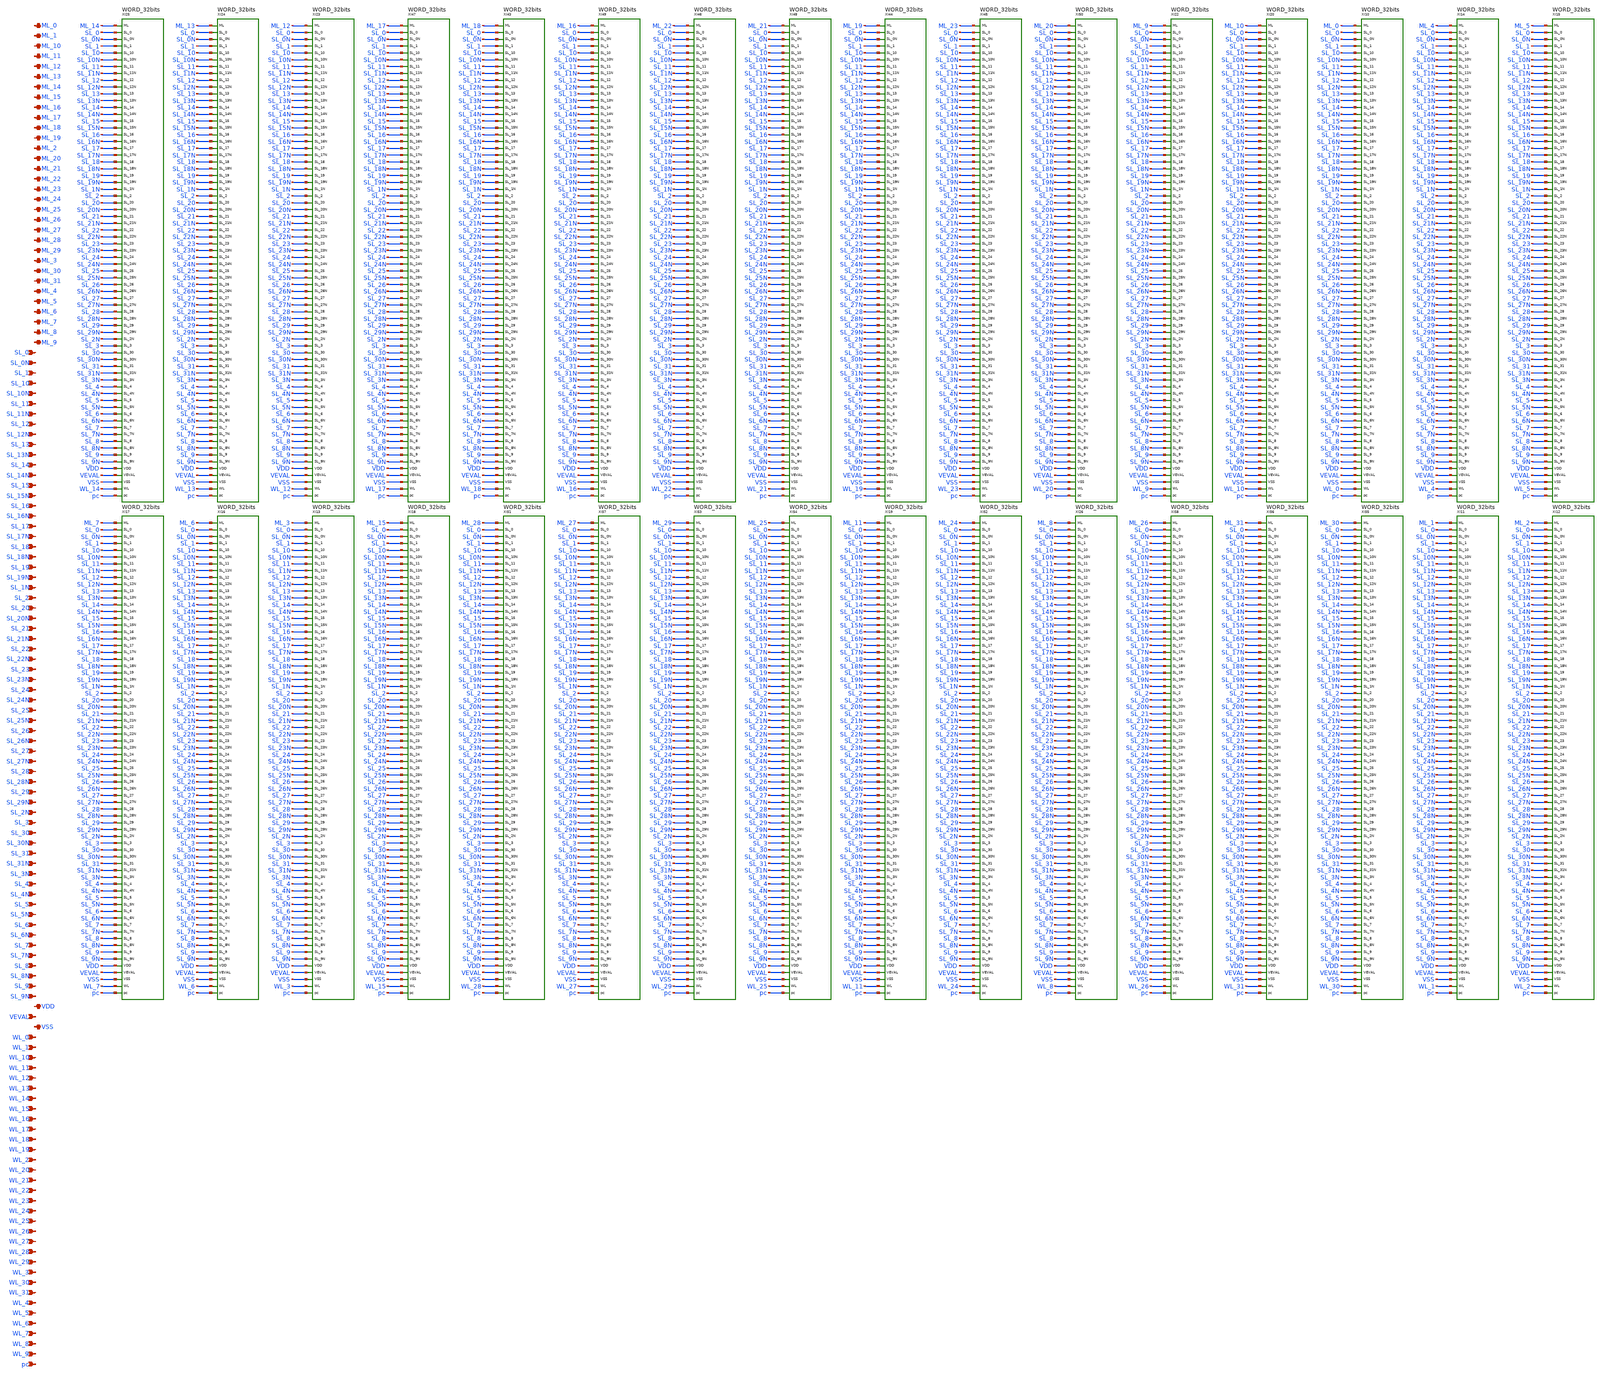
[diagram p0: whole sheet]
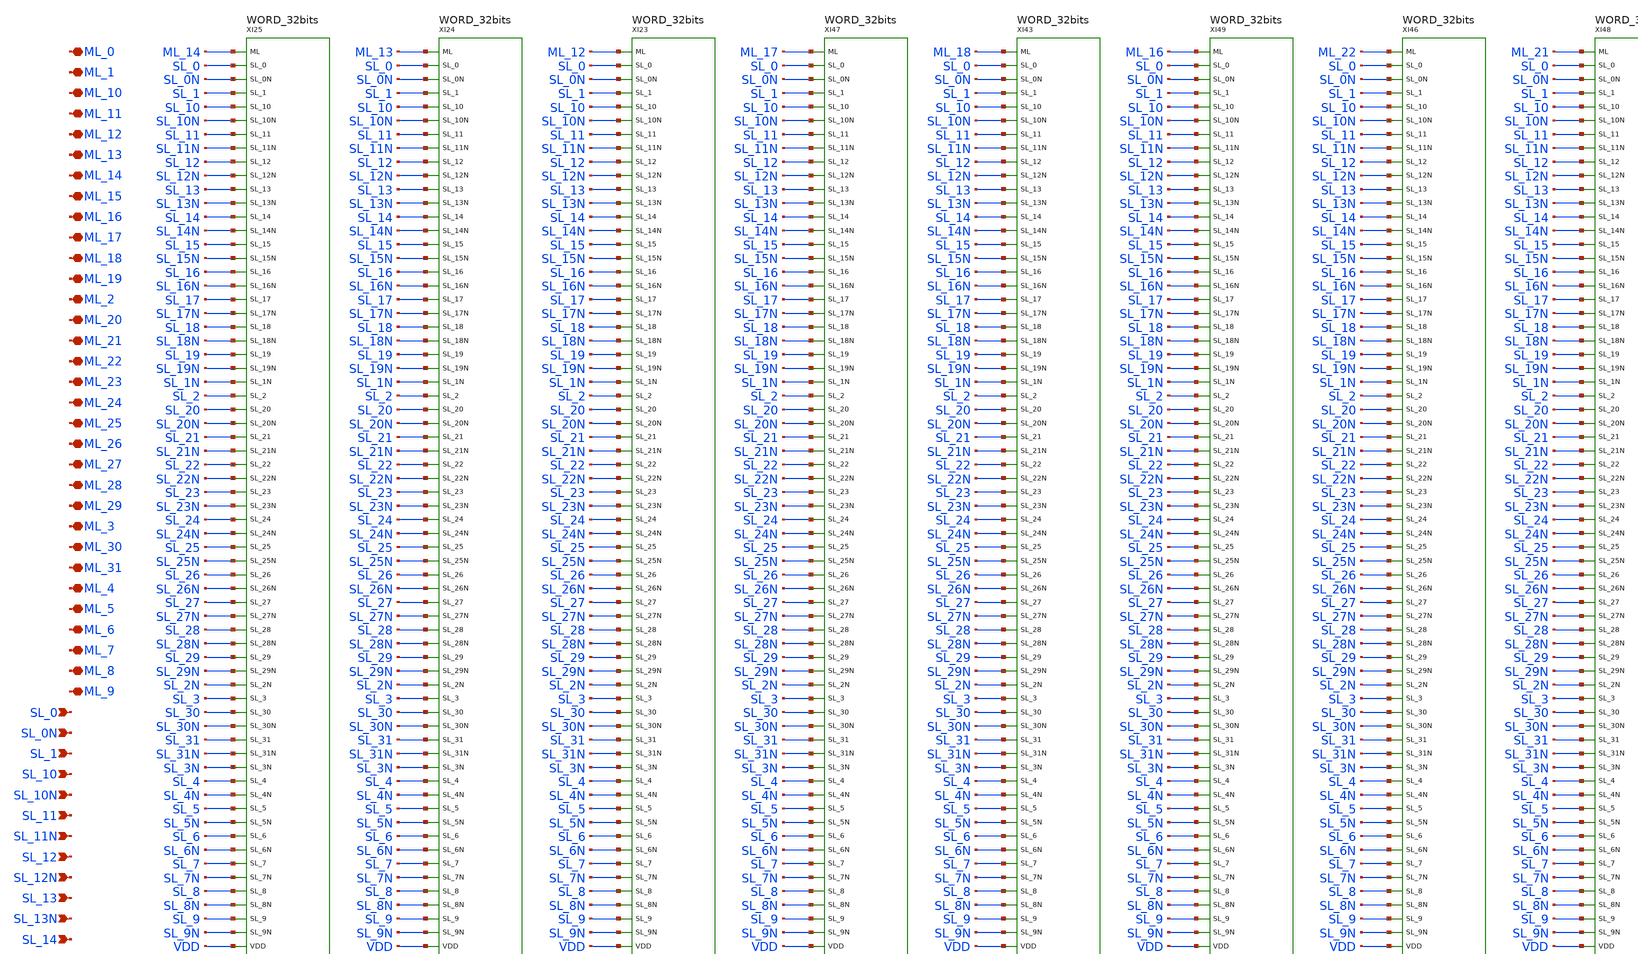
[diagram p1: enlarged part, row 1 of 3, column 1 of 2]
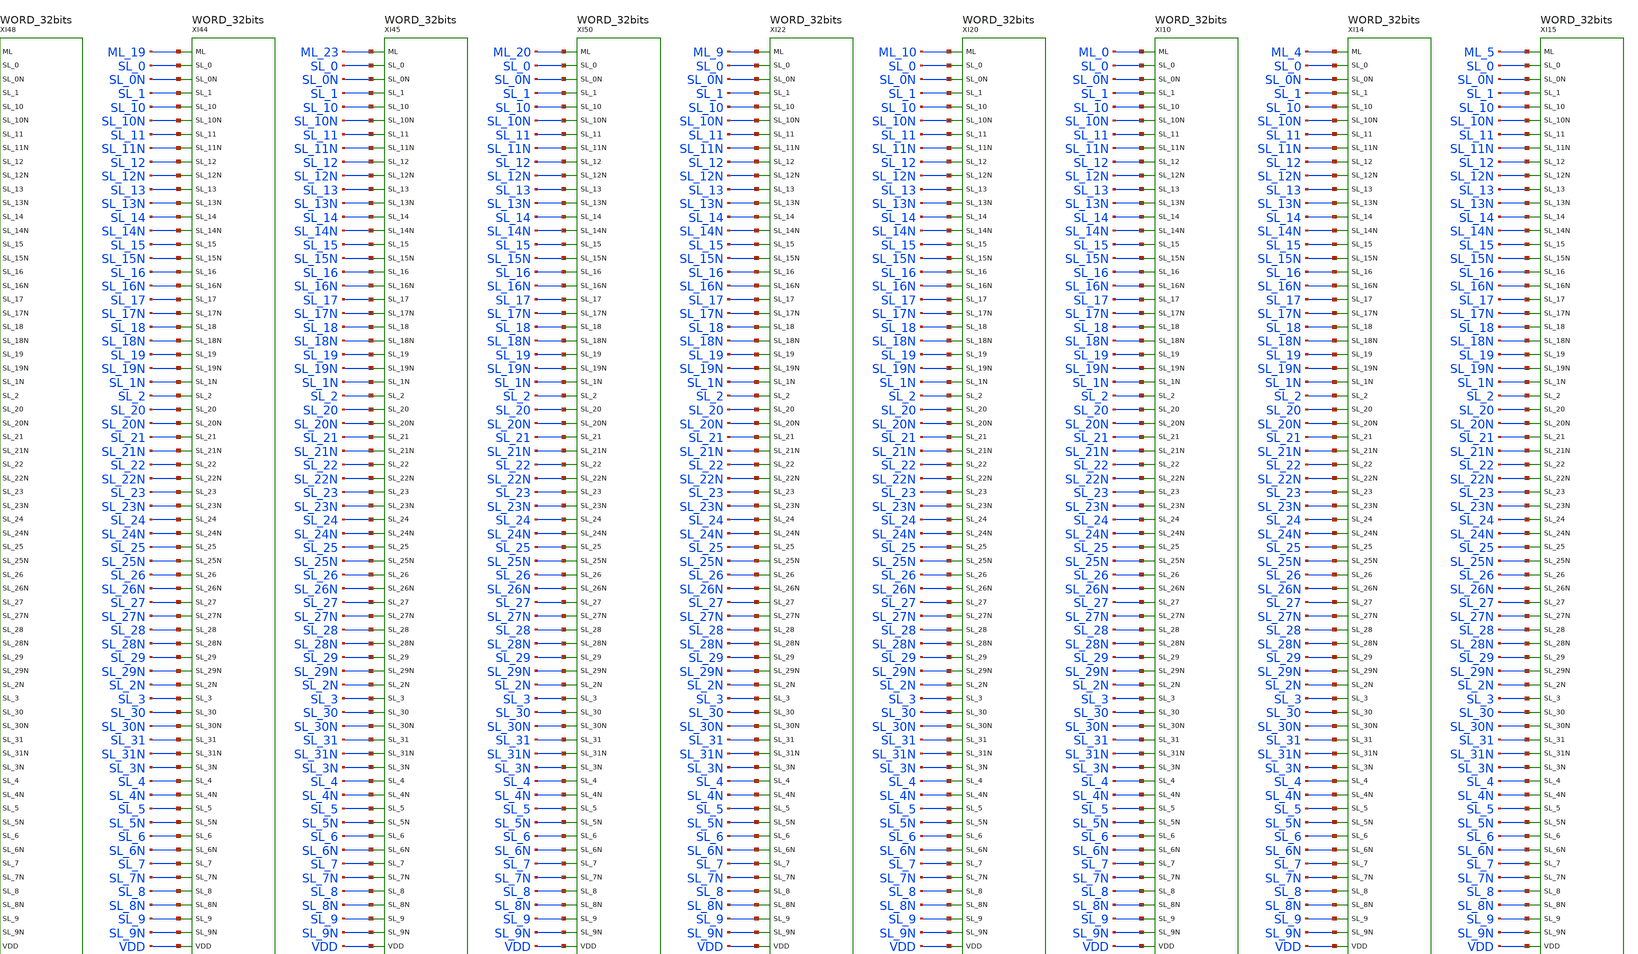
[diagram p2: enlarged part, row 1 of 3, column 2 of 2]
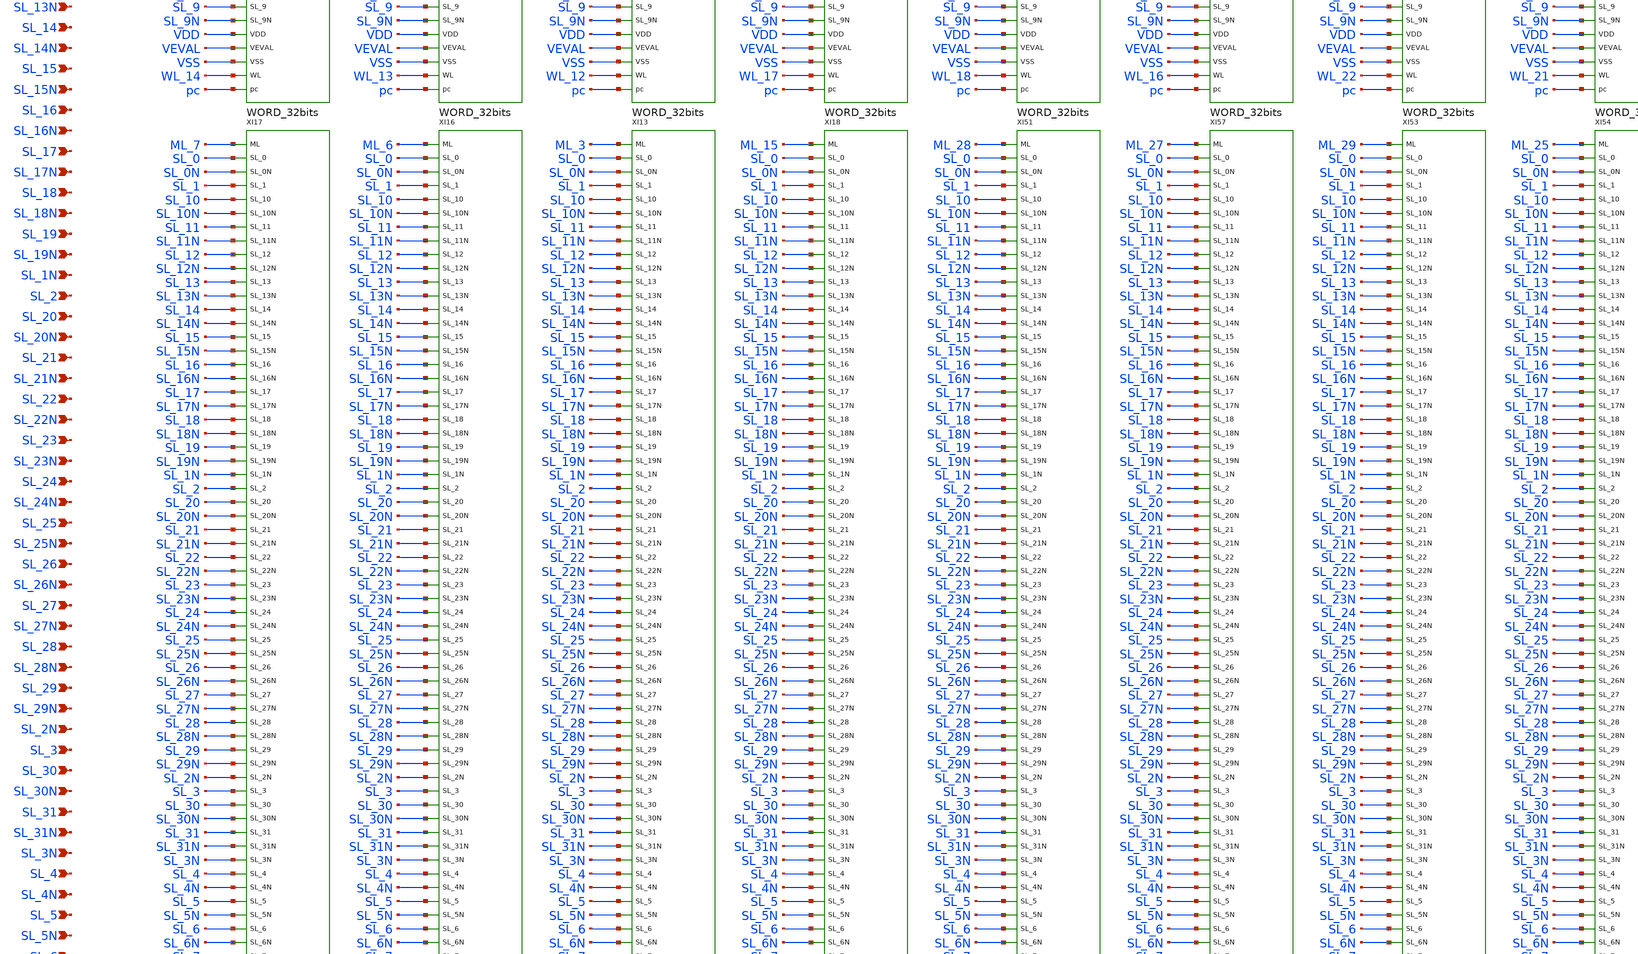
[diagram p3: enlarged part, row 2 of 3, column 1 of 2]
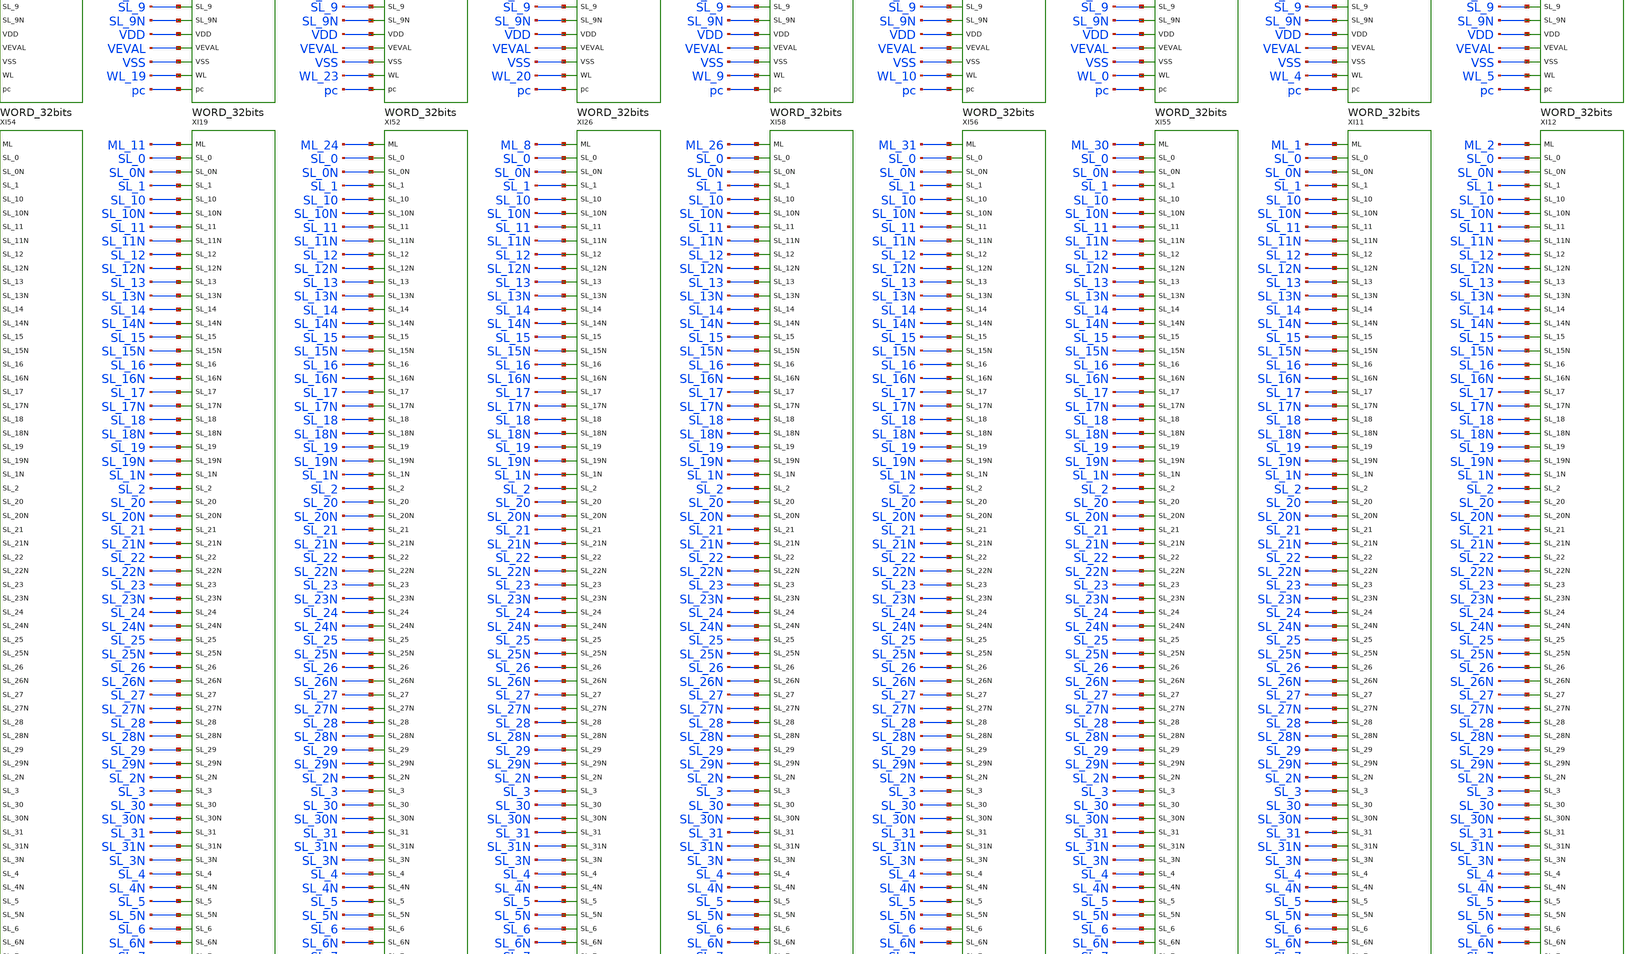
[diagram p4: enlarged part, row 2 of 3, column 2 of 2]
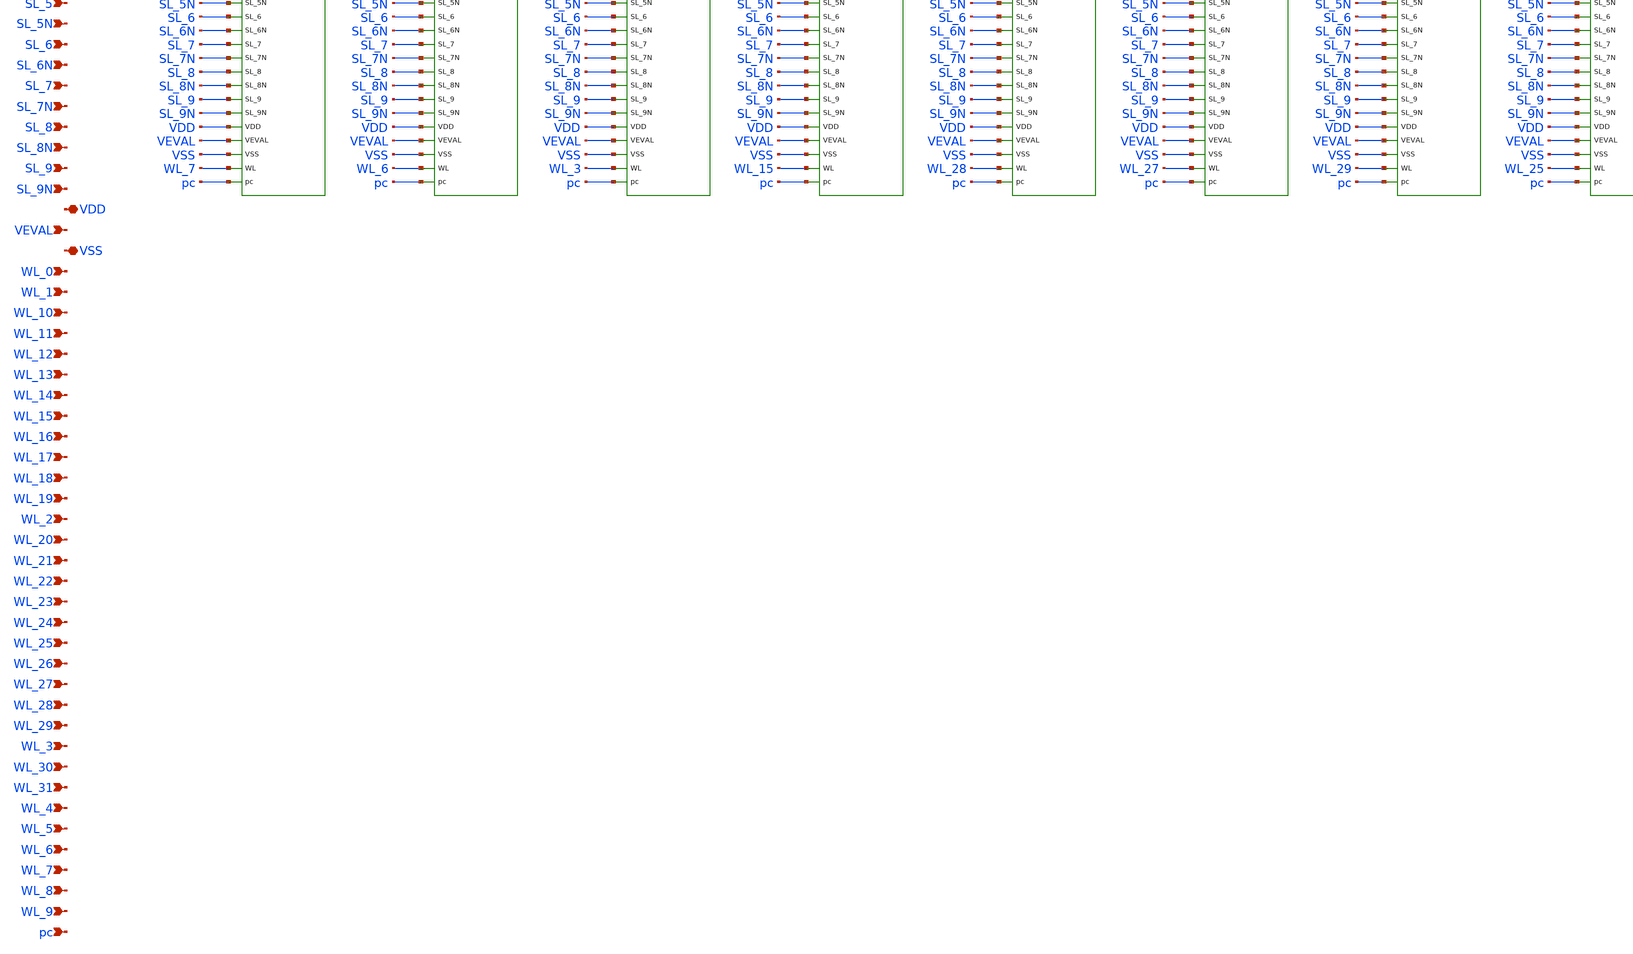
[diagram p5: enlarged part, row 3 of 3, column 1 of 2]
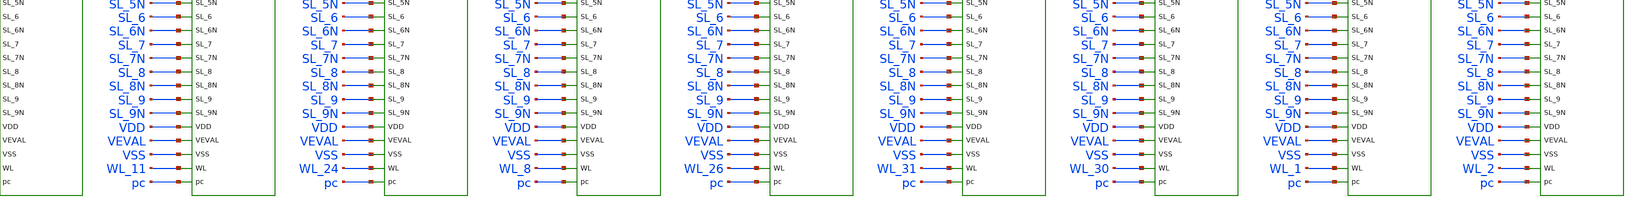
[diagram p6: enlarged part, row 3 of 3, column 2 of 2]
** sch_path: SoC6169-main/schematic/xschem/ARRAY_32x32.sch
* Copyright 2026 USFQ CAM team
* Licensed under the Apache License, Version 2.0 (the "License");
* you may not use this file except in compliance with the License.
* You may obtain a copy of the License at
* https://www.apache.org/licenses/LICENSE-2.0
* Unless required by applicable law or agreed to in writing, software
* distributed under the License is distributed on an "AS IS" BASIS,
* WITHOUT WARRANTIES OR CONDITIONS OF ANY KIND, either express or implied.
* See the License for the specific language governing permissions and
* limitations under the License.
**.subckt ARRAY_32x32 ML_0 ML_1 ML_10 ML_11 ML_12 ML_13 ML_14 ML_15 ML_16 ML_17 ML_18 ML_19 ML_2
*+ ML_20 ML_21 ML_22 ML_23 ML_24 ML_25 ML_26 ML_27 ML_28 ML_29 ML_3 ML_30 ML_31 ML_4 ML_5 ML_6 ML_7 ML_8
*+ ML_9 SL_0 SL_0N SL_1 SL_10 SL_10N SL_11 SL_11N SL_12 SL_12N SL_13 SL_13N SL_14 SL_14N SL_15 SL_15N SL_16
*+ SL_16N SL_17 SL_17N SL_18 SL_18N SL_19 SL_19N SL_1N SL_2 SL_20 SL_20N SL_21 SL_21N SL_22 SL_22N SL_23
*+ SL_23N SL_24 SL_24N SL_25 SL_25N SL_26 SL_26N SL_27 SL_27N SL_28 SL_28N SL_29 SL_29N SL_2N SL_3 SL_30
*+ SL_30N SL_31 SL_31N SL_3N SL_4 SL_4N SL_5 SL_5N SL_6 SL_6N SL_7 SL_7N SL_8 SL_8N SL_9 SL_9N VDD VEVAL VSS
*+ WL_0 WL_1 WL_10 WL_11 WL_12 WL_13 WL_14 WL_15 WL_16 WL_17 WL_18 WL_19 WL_2 WL_20 WL_21 WL_22 WL_23 WL_24
*+ WL_25 WL_26 WL_27 WL_28 WL_29 WL_3 WL_30 WL_31 WL_4 WL_5 WL_6 WL_7 WL_8 WL_9 pc
*.iopin ML_0
*.iopin ML_1
*.iopin ML_10
*.iopin ML_11
*.iopin ML_12
*.iopin ML_13
*.iopin ML_14
*.iopin ML_15
*.iopin ML_16
*.iopin ML_17
*.iopin ML_18
*.iopin ML_19
*.iopin ML_2
*.iopin ML_20
*.iopin ML_21
*.iopin ML_22
*.iopin ML_23
*.iopin ML_24
*.iopin ML_25
*.iopin ML_26
*.iopin ML_27
*.iopin ML_28
*.iopin ML_29
*.iopin ML_3
*.iopin ML_30
*.iopin ML_31
*.iopin ML_4
*.iopin ML_5
*.iopin ML_6
*.iopin ML_7
*.iopin ML_8
*.iopin ML_9
*.ipin SL_0
*.ipin SL_0N
*.ipin SL_1
*.ipin SL_10
*.ipin SL_10N
*.ipin SL_11
*.ipin SL_11N
*.ipin SL_12
*.ipin SL_12N
*.ipin SL_13
*.ipin SL_13N
*.ipin SL_14
*.ipin SL_14N
*.ipin SL_15
*.ipin SL_15N
*.ipin SL_16
*.ipin SL_16N
*.ipin SL_17
*.ipin SL_17N
*.ipin SL_18
*.ipin SL_18N
*.ipin SL_19
*.ipin SL_19N
*.ipin SL_1N
*.ipin SL_2
*.ipin SL_20
*.ipin SL_20N
*.ipin SL_21
*.ipin SL_21N
*.ipin SL_22
*.ipin SL_22N
*.ipin SL_23
*.ipin SL_23N
*.ipin SL_24
*.ipin SL_24N
*.ipin SL_25
*.ipin SL_25N
*.ipin SL_26
*.ipin SL_26N
*.ipin SL_27
*.ipin SL_27N
*.ipin SL_28
*.ipin SL_28N
*.ipin SL_29
*.ipin SL_29N
*.ipin SL_2N
*.ipin SL_3
*.ipin SL_30
*.ipin SL_30N
*.ipin SL_31
*.ipin SL_31N
*.ipin SL_3N
*.ipin SL_4
*.ipin SL_4N
*.ipin SL_5
*.ipin SL_5N
*.ipin SL_6
*.ipin SL_6N
*.ipin SL_7
*.ipin SL_7N
*.ipin SL_8
*.ipin SL_8N
*.ipin SL_9
*.ipin SL_9N
*.iopin VDD
*.ipin VEVAL
*.iopin VSS
*.ipin WL_0
*.ipin WL_1
*.ipin WL_10
*.ipin WL_11
*.ipin WL_12
*.ipin WL_13
*.ipin WL_14
*.ipin WL_15
*.ipin WL_16
*.ipin WL_17
*.ipin WL_18
*.ipin WL_19
*.ipin WL_2
*.ipin WL_20
*.ipin WL_21
*.ipin WL_22
*.ipin WL_23
*.ipin WL_24
*.ipin WL_25
*.ipin WL_26
*.ipin WL_27
*.ipin WL_28
*.ipin WL_29
*.ipin WL_3
*.ipin WL_30
*.ipin WL_31
*.ipin WL_4
*.ipin WL_5
*.ipin WL_6
*.ipin WL_7
*.ipin WL_8
*.ipin WL_9
*.ipin pc
XI25 ML_14 SL_0 SL_0N SL_1 SL_10 SL_10N SL_11 SL_11N SL_12 SL_12N SL_13 SL_13N SL_14 SL_14N SL_15
+ SL_15N SL_16 SL_16N SL_17 SL_17N SL_18 SL_18N SL_19 SL_19N SL_1N SL_2 SL_20 SL_20N SL_21 SL_21N SL_22
+ SL_22N SL_23 SL_23N SL_24 SL_24N SL_25 SL_25N SL_26 SL_26N SL_27 SL_27N SL_28 SL_28N SL_29 SL_29N SL_2N
+ SL_3 SL_30 SL_30N SL_31 SL_31N SL_3N SL_4 SL_4N SL_5 SL_5N SL_6 SL_6N SL_7 SL_7N SL_8 SL_8N SL_9 SL_9N
+ VDD VEVAL VSS WL_14 pc WORD_32bits
XI24 ML_13 SL_0 SL_0N SL_1 SL_10 SL_10N SL_11 SL_11N SL_12 SL_12N SL_13 SL_13N SL_14 SL_14N SL_15
+ SL_15N SL_16 SL_16N SL_17 SL_17N SL_18 SL_18N SL_19 SL_19N SL_1N SL_2 SL_20 SL_20N SL_21 SL_21N SL_22
+ SL_22N SL_23 SL_23N SL_24 SL_24N SL_25 SL_25N SL_26 SL_26N SL_27 SL_27N SL_28 SL_28N SL_29 SL_29N SL_2N
+ SL_3 SL_30 SL_30N SL_31 SL_31N SL_3N SL_4 SL_4N SL_5 SL_5N SL_6 SL_6N SL_7 SL_7N SL_8 SL_8N SL_9 SL_9N
+ VDD VEVAL VSS WL_13 pc WORD_32bits
XI23 ML_12 SL_0 SL_0N SL_1 SL_10 SL_10N SL_11 SL_11N SL_12 SL_12N SL_13 SL_13N SL_14 SL_14N SL_15
+ SL_15N SL_16 SL_16N SL_17 SL_17N SL_18 SL_18N SL_19 SL_19N SL_1N SL_2 SL_20 SL_20N SL_21 SL_21N SL_22
+ SL_22N SL_23 SL_23N SL_24 SL_24N SL_25 SL_25N SL_26 SL_26N SL_27 SL_27N SL_28 SL_28N SL_29 SL_29N SL_2N
+ SL_3 SL_30 SL_30N SL_31 SL_31N SL_3N SL_4 SL_4N SL_5 SL_5N SL_6 SL_6N SL_7 SL_7N SL_8 SL_8N SL_9 SL_9N
+ VDD VEVAL VSS WL_12 pc WORD_32bits
XI47 ML_17 SL_0 SL_0N SL_1 SL_10 SL_10N SL_11 SL_11N SL_12 SL_12N SL_13 SL_13N SL_14 SL_14N SL_15
+ SL_15N SL_16 SL_16N SL_17 SL_17N SL_18 SL_18N SL_19 SL_19N SL_1N SL_2 SL_20 SL_20N SL_21 SL_21N SL_22
+ SL_22N SL_23 SL_23N SL_24 SL_24N SL_25 SL_25N SL_26 SL_26N SL_27 SL_27N SL_28 SL_28N SL_29 SL_29N SL_2N
+ SL_3 SL_30 SL_30N SL_31 SL_31N SL_3N SL_4 SL_4N SL_5 SL_5N SL_6 SL_6N SL_7 SL_7N SL_8 SL_8N SL_9 SL_9N
+ VDD VEVAL VSS WL_17 pc WORD_32bits
XI43 ML_18 SL_0 SL_0N SL_1 SL_10 SL_10N SL_11 SL_11N SL_12 SL_12N SL_13 SL_13N SL_14 SL_14N SL_15
+ SL_15N SL_16 SL_16N SL_17 SL_17N SL_18 SL_18N SL_19 SL_19N SL_1N SL_2 SL_20 SL_20N SL_21 SL_21N SL_22
+ SL_22N SL_23 SL_23N SL_24 SL_24N SL_25 SL_25N SL_26 SL_26N SL_27 SL_27N SL_28 SL_28N SL_29 SL_29N SL_2N
+ SL_3 SL_30 SL_30N SL_31 SL_31N SL_3N SL_4 SL_4N SL_5 SL_5N SL_6 SL_6N SL_7 SL_7N SL_8 SL_8N SL_9 SL_9N
+ VDD VEVAL VSS WL_18 pc WORD_32bits
XI49 ML_16 SL_0 SL_0N SL_1 SL_10 SL_10N SL_11 SL_11N SL_12 SL_12N SL_13 SL_13N SL_14 SL_14N SL_15
+ SL_15N SL_16 SL_16N SL_17 SL_17N SL_18 SL_18N SL_19 SL_19N SL_1N SL_2 SL_20 SL_20N SL_21 SL_21N SL_22
+ SL_22N SL_23 SL_23N SL_24 SL_24N SL_25 SL_25N SL_26 SL_26N SL_27 SL_27N SL_28 SL_28N SL_29 SL_29N SL_2N
+ SL_3 SL_30 SL_30N SL_31 SL_31N SL_3N SL_4 SL_4N SL_5 SL_5N SL_6 SL_6N SL_7 SL_7N SL_8 SL_8N SL_9 SL_9N
+ VDD VEVAL VSS WL_16 pc WORD_32bits
XI46 ML_22 SL_0 SL_0N SL_1 SL_10 SL_10N SL_11 SL_11N SL_12 SL_12N SL_13 SL_13N SL_14 SL_14N SL_15
+ SL_15N SL_16 SL_16N SL_17 SL_17N SL_18 SL_18N SL_19 SL_19N SL_1N SL_2 SL_20 SL_20N SL_21 SL_21N SL_22
+ SL_22N SL_23 SL_23N SL_24 SL_24N SL_25 SL_25N SL_26 SL_26N SL_27 SL_27N SL_28 SL_28N SL_29 SL_29N SL_2N
+ SL_3 SL_30 SL_30N SL_31 SL_31N SL_3N SL_4 SL_4N SL_5 SL_5N SL_6 SL_6N SL_7 SL_7N SL_8 SL_8N SL_9 SL_9N
+ VDD VEVAL VSS WL_22 pc WORD_32bits
XI48 ML_21 SL_0 SL_0N SL_1 SL_10 SL_10N SL_11 SL_11N SL_12 SL_12N SL_13 SL_13N SL_14 SL_14N SL_15
+ SL_15N SL_16 SL_16N SL_17 SL_17N SL_18 SL_18N SL_19 SL_19N SL_1N SL_2 SL_20 SL_20N SL_21 SL_21N SL_22
+ SL_22N SL_23 SL_23N SL_24 SL_24N SL_25 SL_25N SL_26 SL_26N SL_27 SL_27N SL_28 SL_28N SL_29 SL_29N SL_2N
+ SL_3 SL_30 SL_30N SL_31 SL_31N SL_3N SL_4 SL_4N SL_5 SL_5N SL_6 SL_6N SL_7 SL_7N SL_8 SL_8N SL_9 SL_9N
+ VDD VEVAL VSS WL_21 pc WORD_32bits
XI44 ML_19 SL_0 SL_0N SL_1 SL_10 SL_10N SL_11 SL_11N SL_12 SL_12N SL_13 SL_13N SL_14 SL_14N SL_15
+ SL_15N SL_16 SL_16N SL_17 SL_17N SL_18 SL_18N SL_19 SL_19N SL_1N SL_2 SL_20 SL_20N SL_21 SL_21N SL_22
+ SL_22N SL_23 SL_23N SL_24 SL_24N SL_25 SL_25N SL_26 SL_26N SL_27 SL_27N SL_28 SL_28N SL_29 SL_29N SL_2N
+ SL_3 SL_30 SL_30N SL_31 SL_31N SL_3N SL_4 SL_4N SL_5 SL_5N SL_6 SL_6N SL_7 SL_7N SL_8 SL_8N SL_9 SL_9N
+ VDD VEVAL VSS WL_19 pc WORD_32bits
XI45 ML_23 SL_0 SL_0N SL_1 SL_10 SL_10N SL_11 SL_11N SL_12 SL_12N SL_13 SL_13N SL_14 SL_14N SL_15
+ SL_15N SL_16 SL_16N SL_17 SL_17N SL_18 SL_18N SL_19 SL_19N SL_1N SL_2 SL_20 SL_20N SL_21 SL_21N SL_22
+ SL_22N SL_23 SL_23N SL_24 SL_24N SL_25 SL_25N SL_26 SL_26N SL_27 SL_27N SL_28 SL_28N SL_29 SL_29N SL_2N
+ SL_3 SL_30 SL_30N SL_31 SL_31N SL_3N SL_4 SL_4N SL_5 SL_5N SL_6 SL_6N SL_7 SL_7N SL_8 SL_8N SL_9 SL_9N
+ VDD VEVAL VSS WL_23 pc WORD_32bits
XI50 ML_20 SL_0 SL_0N SL_1 SL_10 SL_10N SL_11 SL_11N SL_12 SL_12N SL_13 SL_13N SL_14 SL_14N SL_15
+ SL_15N SL_16 SL_16N SL_17 SL_17N SL_18 SL_18N SL_19 SL_19N SL_1N SL_2 SL_20 SL_20N SL_21 SL_21N SL_22
+ SL_22N SL_23 SL_23N SL_24 SL_24N SL_25 SL_25N SL_26 SL_26N SL_27 SL_27N SL_28 SL_28N SL_29 SL_29N SL_2N
+ SL_3 SL_30 SL_30N SL_31 SL_31N SL_3N SL_4 SL_4N SL_5 SL_5N SL_6 SL_6N SL_7 SL_7N SL_8 SL_8N SL_9 SL_9N
+ VDD VEVAL VSS WL_20 pc WORD_32bits
XI22 ML_9 SL_0 SL_0N SL_1 SL_10 SL_10N SL_11 SL_11N SL_12 SL_12N SL_13 SL_13N SL_14 SL_14N SL_15
+ SL_15N SL_16 SL_16N SL_17 SL_17N SL_18 SL_18N SL_19 SL_19N SL_1N SL_2 SL_20 SL_20N SL_21 SL_21N SL_22
+ SL_22N SL_23 SL_23N SL_24 SL_24N SL_25 SL_25N SL_26 SL_26N SL_27 SL_27N SL_28 SL_28N SL_29 SL_29N SL_2N
+ SL_3 SL_30 SL_30N SL_31 SL_31N SL_3N SL_4 SL_4N SL_5 SL_5N SL_6 SL_6N SL_7 SL_7N SL_8 SL_8N SL_9 SL_9N
+ VDD VEVAL VSS WL_9 pc WORD_32bits
XI20 ML_10 SL_0 SL_0N SL_1 SL_10 SL_10N SL_11 SL_11N SL_12 SL_12N SL_13 SL_13N SL_14 SL_14N SL_15
+ SL_15N SL_16 SL_16N SL_17 SL_17N SL_18 SL_18N SL_19 SL_19N SL_1N SL_2 SL_20 SL_20N SL_21 SL_21N SL_22
+ SL_22N SL_23 SL_23N SL_24 SL_24N SL_25 SL_25N SL_26 SL_26N SL_27 SL_27N SL_28 SL_28N SL_29 SL_29N SL_2N
+ SL_3 SL_30 SL_30N SL_31 SL_31N SL_3N SL_4 SL_4N SL_5 SL_5N SL_6 SL_6N SL_7 SL_7N SL_8 SL_8N SL_9 SL_9N
+ VDD VEVAL VSS WL_10 pc WORD_32bits
XI10 ML_0 SL_0 SL_0N SL_1 SL_10 SL_10N SL_11 SL_11N SL_12 SL_12N SL_13 SL_13N SL_14 SL_14N SL_15
+ SL_15N SL_16 SL_16N SL_17 SL_17N SL_18 SL_18N SL_19 SL_19N SL_1N SL_2 SL_20 SL_20N SL_21 SL_21N SL_22
+ SL_22N SL_23 SL_23N SL_24 SL_24N SL_25 SL_25N SL_26 SL_26N SL_27 SL_27N SL_28 SL_28N SL_29 SL_29N SL_2N
+ SL_3 SL_30 SL_30N SL_31 SL_31N SL_3N SL_4 SL_4N SL_5 SL_5N SL_6 SL_6N SL_7 SL_7N SL_8 SL_8N SL_9 SL_9N
+ VDD VEVAL VSS WL_0 pc WORD_32bits
XI14 ML_4 SL_0 SL_0N SL_1 SL_10 SL_10N SL_11 SL_11N SL_12 SL_12N SL_13 SL_13N SL_14 SL_14N SL_15
+ SL_15N SL_16 SL_16N SL_17 SL_17N SL_18 SL_18N SL_19 SL_19N SL_1N SL_2 SL_20 SL_20N SL_21 SL_21N SL_22
+ SL_22N SL_23 SL_23N SL_24 SL_24N SL_25 SL_25N SL_26 SL_26N SL_27 SL_27N SL_28 SL_28N SL_29 SL_29N SL_2N
+ SL_3 SL_30 SL_30N SL_31 SL_31N SL_3N SL_4 SL_4N SL_5 SL_5N SL_6 SL_6N SL_7 SL_7N SL_8 SL_8N SL_9 SL_9N
+ VDD VEVAL VSS WL_4 pc WORD_32bits
XI15 ML_5 SL_0 SL_0N SL_1 SL_10 SL_10N SL_11 SL_11N SL_12 SL_12N SL_13 SL_13N SL_14 SL_14N SL_15
+ SL_15N SL_16 SL_16N SL_17 SL_17N SL_18 SL_18N SL_19 SL_19N SL_1N SL_2 SL_20 SL_20N SL_21 SL_21N SL_22
+ SL_22N SL_23 SL_23N SL_24 SL_24N SL_25 SL_25N SL_26 SL_26N SL_27 SL_27N SL_28 SL_28N SL_29 SL_29N SL_2N
+ SL_3 SL_30 SL_30N SL_31 SL_31N SL_3N SL_4 SL_4N SL_5 SL_5N SL_6 SL_6N SL_7 SL_7N SL_8 SL_8N SL_9 SL_9N
+ VDD VEVAL VSS WL_5 pc WORD_32bits
XI17 ML_7 SL_0 SL_0N SL_1 SL_10 SL_10N SL_11 SL_11N SL_12 SL_12N SL_13 SL_13N SL_14 SL_14N SL_15
+ SL_15N SL_16 SL_16N SL_17 SL_17N SL_18 SL_18N SL_19 SL_19N SL_1N SL_2 SL_20 SL_20N SL_21 SL_21N SL_22
+ SL_22N SL_23 SL_23N SL_24 SL_24N SL_25 SL_25N SL_26 SL_26N SL_27 SL_27N SL_28 SL_28N SL_29 SL_29N SL_2N
+ SL_3 SL_30 SL_30N SL_31 SL_31N SL_3N SL_4 SL_4N SL_5 SL_5N SL_6 SL_6N SL_7 SL_7N SL_8 SL_8N SL_9 SL_9N
+ VDD VEVAL VSS WL_7 pc WORD_32bits
XI16 ML_6 SL_0 SL_0N SL_1 SL_10 SL_10N SL_11 SL_11N SL_12 SL_12N SL_13 SL_13N SL_14 SL_14N SL_15
+ SL_15N SL_16 SL_16N SL_17 SL_17N SL_18 SL_18N SL_19 SL_19N SL_1N SL_2 SL_20 SL_20N SL_21 SL_21N SL_22
+ SL_22N SL_23 SL_23N SL_24 SL_24N SL_25 SL_25N SL_26 SL_26N SL_27 SL_27N SL_28 SL_28N SL_29 SL_29N SL_2N
+ SL_3 SL_30 SL_30N SL_31 SL_31N SL_3N SL_4 SL_4N SL_5 SL_5N SL_6 SL_6N SL_7 SL_7N SL_8 SL_8N SL_9 SL_9N
+ VDD VEVAL VSS WL_6 pc WORD_32bits
XI13 ML_3 SL_0 SL_0N SL_1 SL_10 SL_10N SL_11 SL_11N SL_12 SL_12N SL_13 SL_13N SL_14 SL_14N SL_15
+ SL_15N SL_16 SL_16N SL_17 SL_17N SL_18 SL_18N SL_19 SL_19N SL_1N SL_2 SL_20 SL_20N SL_21 SL_21N SL_22
+ SL_22N SL_23 SL_23N SL_24 SL_24N SL_25 SL_25N SL_26 SL_26N SL_27 SL_27N SL_28 SL_28N SL_29 SL_29N SL_2N
+ SL_3 SL_30 SL_30N SL_31 SL_31N SL_3N SL_4 SL_4N SL_5 SL_5N SL_6 SL_6N SL_7 SL_7N SL_8 SL_8N SL_9 SL_9N
+ VDD VEVAL VSS WL_3 pc WORD_32bits
XI18 ML_15 SL_0 SL_0N SL_1 SL_10 SL_10N SL_11 SL_11N SL_12 SL_12N SL_13 SL_13N SL_14 SL_14N SL_15
+ SL_15N SL_16 SL_16N SL_17 SL_17N SL_18 SL_18N SL_19 SL_19N SL_1N SL_2 SL_20 SL_20N SL_21 SL_21N SL_22
+ SL_22N SL_23 SL_23N SL_24 SL_24N SL_25 SL_25N SL_26 SL_26N SL_27 SL_27N SL_28 SL_28N SL_29 SL_29N SL_2N
+ SL_3 SL_30 SL_30N SL_31 SL_31N SL_3N SL_4 SL_4N SL_5 SL_5N SL_6 SL_6N SL_7 SL_7N SL_8 SL_8N SL_9 SL_9N
+ VDD VEVAL VSS WL_15 pc WORD_32bits
XI51 ML_28 SL_0 SL_0N SL_1 SL_10 SL_10N SL_11 SL_11N SL_12 SL_12N SL_13 SL_13N SL_14 SL_14N SL_15
+ SL_15N SL_16 SL_16N SL_17 SL_17N SL_18 SL_18N SL_19 SL_19N SL_1N SL_2 SL_20 SL_20N SL_21 SL_21N SL_22
+ SL_22N SL_23 SL_23N SL_24 SL_24N SL_25 SL_25N SL_26 SL_26N SL_27 SL_27N SL_28 SL_28N SL_29 SL_29N SL_2N
+ SL_3 SL_30 SL_30N SL_31 SL_31N SL_3N SL_4 SL_4N SL_5 SL_5N SL_6 SL_6N SL_7 SL_7N SL_8 SL_8N SL_9 SL_9N
+ VDD VEVAL VSS WL_28 pc WORD_32bits
XI57 ML_27 SL_0 SL_0N SL_1 SL_10 SL_10N SL_11 SL_11N SL_12 SL_12N SL_13 SL_13N SL_14 SL_14N SL_15
+ SL_15N SL_16 SL_16N SL_17 SL_17N SL_18 SL_18N SL_19 SL_19N SL_1N SL_2 SL_20 SL_20N SL_21 SL_21N SL_22
+ SL_22N SL_23 SL_23N SL_24 SL_24N SL_25 SL_25N SL_26 SL_26N SL_27 SL_27N SL_28 SL_28N SL_29 SL_29N SL_2N
+ SL_3 SL_30 SL_30N SL_31 SL_31N SL_3N SL_4 SL_4N SL_5 SL_5N SL_6 SL_6N SL_7 SL_7N SL_8 SL_8N SL_9 SL_9N
+ VDD VEVAL VSS WL_27 pc WORD_32bits
XI53 ML_29 SL_0 SL_0N SL_1 SL_10 SL_10N SL_11 SL_11N SL_12 SL_12N SL_13 SL_13N SL_14 SL_14N SL_15
+ SL_15N SL_16 SL_16N SL_17 SL_17N SL_18 SL_18N SL_19 SL_19N SL_1N SL_2 SL_20 SL_20N SL_21 SL_21N SL_22
+ SL_22N SL_23 SL_23N SL_24 SL_24N SL_25 SL_25N SL_26 SL_26N SL_27 SL_27N SL_28 SL_28N SL_29 SL_29N SL_2N
+ SL_3 SL_30 SL_30N SL_31 SL_31N SL_3N SL_4 SL_4N SL_5 SL_5N SL_6 SL_6N SL_7 SL_7N SL_8 SL_8N SL_9 SL_9N
+ VDD VEVAL VSS WL_29 pc WORD_32bits
XI54 ML_25 SL_0 SL_0N SL_1 SL_10 SL_10N SL_11 SL_11N SL_12 SL_12N SL_13 SL_13N SL_14 SL_14N SL_15
+ SL_15N SL_16 SL_16N SL_17 SL_17N SL_18 SL_18N SL_19 SL_19N SL_1N SL_2 SL_20 SL_20N SL_21 SL_21N SL_22
+ SL_22N SL_23 SL_23N SL_24 SL_24N SL_25 SL_25N SL_26 SL_26N SL_27 SL_27N SL_28 SL_28N SL_29 SL_29N SL_2N
+ SL_3 SL_30 SL_30N SL_31 SL_31N SL_3N SL_4 SL_4N SL_5 SL_5N SL_6 SL_6N SL_7 SL_7N SL_8 SL_8N SL_9 SL_9N
+ VDD VEVAL VSS WL_25 pc WORD_32bits
XI19 ML_11 SL_0 SL_0N SL_1 SL_10 SL_10N SL_11 SL_11N SL_12 SL_12N SL_13 SL_13N SL_14 SL_14N SL_15
+ SL_15N SL_16 SL_16N SL_17 SL_17N SL_18 SL_18N SL_19 SL_19N SL_1N SL_2 SL_20 SL_20N SL_21 SL_21N SL_22
+ SL_22N SL_23 SL_23N SL_24 SL_24N SL_25 SL_25N SL_26 SL_26N SL_27 SL_27N SL_28 SL_28N SL_29 SL_29N SL_2N
+ SL_3 SL_30 SL_30N SL_31 SL_31N SL_3N SL_4 SL_4N SL_5 SL_5N SL_6 SL_6N SL_7 SL_7N SL_8 SL_8N SL_9 SL_9N
+ VDD VEVAL VSS WL_11 pc WORD_32bits
XI52 ML_24 SL_0 SL_0N SL_1 SL_10 SL_10N SL_11 SL_11N SL_12 SL_12N SL_13 SL_13N SL_14 SL_14N SL_15
+ SL_15N SL_16 SL_16N SL_17 SL_17N SL_18 SL_18N SL_19 SL_19N SL_1N SL_2 SL_20 SL_20N SL_21 SL_21N SL_22
+ SL_22N SL_23 SL_23N SL_24 SL_24N SL_25 SL_25N SL_26 SL_26N SL_27 SL_27N SL_28 SL_28N SL_29 SL_29N SL_2N
+ SL_3 SL_30 SL_30N SL_31 SL_31N SL_3N SL_4 SL_4N SL_5 SL_5N SL_6 SL_6N SL_7 SL_7N SL_8 SL_8N SL_9 SL_9N
+ VDD VEVAL VSS WL_24 pc WORD_32bits
XI26 ML_8 SL_0 SL_0N SL_1 SL_10 SL_10N SL_11 SL_11N SL_12 SL_12N SL_13 SL_13N SL_14 SL_14N SL_15
+ SL_15N SL_16 SL_16N SL_17 SL_17N SL_18 SL_18N SL_19 SL_19N SL_1N SL_2 SL_20 SL_20N SL_21 SL_21N SL_22
+ SL_22N SL_23 SL_23N SL_24 SL_24N SL_25 SL_25N SL_26 SL_26N SL_27 SL_27N SL_28 SL_28N SL_29 SL_29N SL_2N
+ SL_3 SL_30 SL_30N SL_31 SL_31N SL_3N SL_4 SL_4N SL_5 SL_5N SL_6 SL_6N SL_7 SL_7N SL_8 SL_8N SL_9 SL_9N
+ VDD VEVAL VSS WL_8 pc WORD_32bits
XI58 ML_26 SL_0 SL_0N SL_1 SL_10 SL_10N SL_11 SL_11N SL_12 SL_12N SL_13 SL_13N SL_14 SL_14N SL_15
+ SL_15N SL_16 SL_16N SL_17 SL_17N SL_18 SL_18N SL_19 SL_19N SL_1N SL_2 SL_20 SL_20N SL_21 SL_21N SL_22
+ SL_22N SL_23 SL_23N SL_24 SL_24N SL_25 SL_25N SL_26 SL_26N SL_27 SL_27N SL_28 SL_28N SL_29 SL_29N SL_2N
+ SL_3 SL_30 SL_30N SL_31 SL_31N SL_3N SL_4 SL_4N SL_5 SL_5N SL_6 SL_6N SL_7 SL_7N SL_8 SL_8N SL_9 SL_9N
+ VDD VEVAL VSS WL_26 pc WORD_32bits
XI56 ML_31 SL_0 SL_0N SL_1 SL_10 SL_10N SL_11 SL_11N SL_12 SL_12N SL_13 SL_13N SL_14 SL_14N SL_15
+ SL_15N SL_16 SL_16N SL_17 SL_17N SL_18 SL_18N SL_19 SL_19N SL_1N SL_2 SL_20 SL_20N SL_21 SL_21N SL_22
+ SL_22N SL_23 SL_23N SL_24 SL_24N SL_25 SL_25N SL_26 SL_26N SL_27 SL_27N SL_28 SL_28N SL_29 SL_29N SL_2N
+ SL_3 SL_30 SL_30N SL_31 SL_31N SL_3N SL_4 SL_4N SL_5 SL_5N SL_6 SL_6N SL_7 SL_7N SL_8 SL_8N SL_9 SL_9N
+ VDD VEVAL VSS WL_31 pc WORD_32bits
XI55 ML_30 SL_0 SL_0N SL_1 SL_10 SL_10N SL_11 SL_11N SL_12 SL_12N SL_13 SL_13N SL_14 SL_14N SL_15
+ SL_15N SL_16 SL_16N SL_17 SL_17N SL_18 SL_18N SL_19 SL_19N SL_1N SL_2 SL_20 SL_20N SL_21 SL_21N SL_22
+ SL_22N SL_23 SL_23N SL_24 SL_24N SL_25 SL_25N SL_26 SL_26N SL_27 SL_27N SL_28 SL_28N SL_29 SL_29N SL_2N
+ SL_3 SL_30 SL_30N SL_31 SL_31N SL_3N SL_4 SL_4N SL_5 SL_5N SL_6 SL_6N SL_7 SL_7N SL_8 SL_8N SL_9 SL_9N
+ VDD VEVAL VSS WL_30 pc WORD_32bits
XI11 ML_1 SL_0 SL_0N SL_1 SL_10 SL_10N SL_11 SL_11N SL_12 SL_12N SL_13 SL_13N SL_14 SL_14N SL_15
+ SL_15N SL_16 SL_16N SL_17 SL_17N SL_18 SL_18N SL_19 SL_19N SL_1N SL_2 SL_20 SL_20N SL_21 SL_21N SL_22
+ SL_22N SL_23 SL_23N SL_24 SL_24N SL_25 SL_25N SL_26 SL_26N SL_27 SL_27N SL_28 SL_28N SL_29 SL_29N SL_2N
+ SL_3 SL_30 SL_30N SL_31 SL_31N SL_3N SL_4 SL_4N SL_5 SL_5N SL_6 SL_6N SL_7 SL_7N SL_8 SL_8N SL_9 SL_9N
+ VDD VEVAL VSS WL_1 pc WORD_32bits
XI12 ML_2 SL_0 SL_0N SL_1 SL_10 SL_10N SL_11 SL_11N SL_12 SL_12N SL_13 SL_13N SL_14 SL_14N SL_15
+ SL_15N SL_16 SL_16N SL_17 SL_17N SL_18 SL_18N SL_19 SL_19N SL_1N SL_2 SL_20 SL_20N SL_21 SL_21N SL_22
+ SL_22N SL_23 SL_23N SL_24 SL_24N SL_25 SL_25N SL_26 SL_26N SL_27 SL_27N SL_28 SL_28N SL_29 SL_29N SL_2N
+ SL_3 SL_30 SL_30N SL_31 SL_31N SL_3N SL_4 SL_4N SL_5 SL_5N SL_6 SL_6N SL_7 SL_7N SL_8 SL_8N SL_9 SL_9N
+ VDD VEVAL VSS WL_2 pc WORD_32bits
**.ends

* expanding   symbol:  WORD_32bits.sym # of pins=70
** sym_path: SoC6169-main/schematic/xschem/WORD_32bits.sym
** sch_path: SoC6169-main/schematic/xschem/WORD_32bits.sch
.subckt WORD_32bits ML SL_0 SL_0N SL_1 SL_10 SL_10N SL_11 SL_11N SL_12 SL_12N SL_13 SL_13N SL_14
+ SL_14N SL_15 SL_15N SL_16 SL_16N SL_17 SL_17N SL_18 SL_18N SL_19 SL_19N SL_1N SL_2 SL_20 SL_20N SL_21
+ SL_21N SL_22 SL_22N SL_23 SL_23N SL_24 SL_24N SL_25 SL_25N SL_26 SL_26N SL_27 SL_27N SL_28 SL_28N SL_29
+ SL_29N SL_2N SL_3 SL_30 SL_30N SL_31 SL_31N SL_3N SL_4 SL_4N SL_5 SL_5N SL_6 SL_6N SL_7 SL_7N SL_8 SL_8N
+ SL_9 SL_9N VDD VEVAL VSS WL pc
*.iopin ML
*.ipin SL_0
*.ipin SL_0N
*.ipin SL_1
*.ipin SL_10
*.ipin SL_10N
*.ipin SL_11
*.ipin SL_11N
*.ipin SL_12
*.ipin SL_12N
*.ipin SL_13
*.ipin SL_13N
*.ipin SL_14
*.ipin SL_14N
*.ipin SL_15
*.ipin SL_15N
*.ipin SL_16
*.ipin SL_16N
*.ipin SL_17
*.ipin SL_17N
*.ipin SL_18
*.ipin SL_18N
*.ipin SL_19
*.ipin SL_19N
*.ipin SL_1N
*.ipin SL_2
*.ipin SL_20
*.ipin SL_20N
*.ipin SL_21
*.ipin SL_21N
*.ipin SL_22
*.ipin SL_22N
*.ipin SL_23
*.ipin SL_23N
*.ipin SL_24
*.ipin SL_24N
*.ipin SL_25
*.ipin SL_25N
*.ipin SL_26
*.ipin SL_26N
*.ipin SL_27
*.ipin SL_27N
*.ipin SL_28
*.ipin SL_28N
*.ipin SL_29
*.ipin SL_29N
*.ipin SL_2N
*.ipin SL_3
*.ipin SL_30
*.ipin SL_30N
*.ipin SL_31
*.ipin SL_31N
*.ipin SL_3N
*.ipin SL_4
*.ipin SL_4N
*.ipin SL_5
*.ipin SL_5N
*.ipin SL_6
*.ipin SL_6N
*.ipin SL_7
*.ipin SL_7N
*.ipin SL_8
*.ipin SL_8N
*.ipin SL_9
*.ipin SL_9N
*.iopin VDD
*.ipin VEVAL
*.iopin VSS
*.ipin WL
*.ipin pc
XI31 ML SL_27 SL_27N VDD VEVAL VSS WL CELL
XI30 ML SL_24 SL_24N VDD VEVAL VSS WL CELL
XI29 ML SL_25 SL_25N VDD VEVAL VSS WL CELL
XI28 ML SL_26 SL_26N VDD VEVAL VSS WL CELL
XI27 ML SL_28 SL_28N VDD VEVAL VSS WL CELL
XI26 ML SL_29 SL_29N VDD VEVAL VSS WL CELL
XI25 ML SL_30 SL_30N VDD VEVAL VSS WL CELL
XI24 ML SL_31 SL_31N VDD VEVAL VSS WL CELL
XI23 ML SL_19 SL_19N VDD VEVAL VSS WL CELL
XI22 ML SL_16 SL_16N VDD VEVAL VSS WL CELL
XI21 ML SL_17 SL_17N VDD VEVAL VSS WL CELL
XI20 ML SL_18 SL_18N VDD VEVAL VSS WL CELL
XI19 ML SL_20 SL_20N VDD VEVAL VSS WL CELL
XI18 ML SL_21 SL_21N VDD VEVAL VSS WL CELL
XI17 ML SL_22 SL_22N VDD VEVAL VSS WL CELL
XI15 ML SL_11 SL_11N VDD VEVAL VSS WL CELL
XI14 ML SL_8 SL_8N VDD VEVAL VSS WL CELL
XI13 ML SL_9 SL_9N VDD VEVAL VSS WL CELL
XI12 ML SL_10 SL_10N VDD VEVAL VSS WL CELL
XI10 ML SL_12 SL_12N VDD VEVAL VSS WL CELL
XI6 ML SL_13 SL_13N VDD VEVAL VSS WL CELL
XI2 ML SL_14 SL_14N VDD VEVAL VSS WL CELL
XI1 ML SL_15 SL_15N VDD VEVAL VSS WL CELL
XI11 ML SL_3 SL_3N VDD VEVAL VSS WL CELL
XI9 ML SL_0 SL_0N VDD VEVAL VSS WL CELL
XI8 ML SL_1 SL_1N VDD VEVAL VSS WL CELL
XI7 ML SL_2 SL_2N VDD VEVAL VSS WL CELL
XI5 ML SL_4 SL_4N VDD VEVAL VSS WL CELL
XI4 ML SL_5 SL_5N VDD VEVAL VSS WL CELL
XI3 ML SL_6 SL_6N VDD VEVAL VSS WL CELL
XI0 ML SL_7 SL_7N VDD VEVAL VSS WL CELL
XI16 ML SL_23 SL_23N VDD VEVAL VSS WL CELL
XMP0 ML pc VDD VDD sg13_lv_pmos w=2u l=130n ng=1 m=1 mm_ok=1
.ends


* expanding   symbol:  CELL.sym # of pins=7
** sym_path: SoC6169-main/schematic/xschem/CELL.sym
** sch_path: SoC6169-main/schematic/xschem/CELL.sch
.subckt CELL ML SL SL_N VDD VEVAL VSS WL
*.iopin ML
*.ipin SL
*.ipin SL_N
*.iopin VDD
*.ipin VEVAL
*.iopin VSS
*.ipin WL
XI7 VSS net1 VDD net2 INV
XI4 VSS net2 VDD net1 INV
XMN5 net11 VEVAL VSS VSS sg13_lv_nmos w=350n l=130n ng=1 m=1 mm_ok=1
XMN4 net11 net3 ML VSS sg13_lv_nmos w=740n l=130n ng=1 m=1 mm_ok=1
XMN3 net3 net2 SL VSS sg13_lv_nmos w=740n l=130n ng=1 m=1 mm_ok=1
XMN2 net3 net1 SL_N VSS sg13_lv_nmos w=740n l=130n ng=1 m=1 mm_ok=1
XMN1 SL_N WL net1 VSS sg13_lv_nmos w=740n l=130n ng=1 m=1 mm_ok=1
XMN0 SL WL net2 VSS sg13_lv_nmos w=740n l=130n ng=1 m=1 mm_ok=1
.ends


* expanding   symbol:  INV.sym # of pins=4
** sym_path: SoC6169-main/schematic/xschem/INV.sym
** sch_path: SoC6169-main/schematic/xschem/INV.sch
.subckt INV GND IN VDD Y
*.iopin GND
*.ipin IN
*.iopin VDD
*.opin Y
XMN0 Y IN GND GND sg13_lv_nmos w=200n l=130n ng=1 m=1 mm_ok=1
XMP0 Y IN VDD VDD sg13_lv_pmos w=400n l=130n ng=1 m=1 mm_ok=1
.ends

.end
